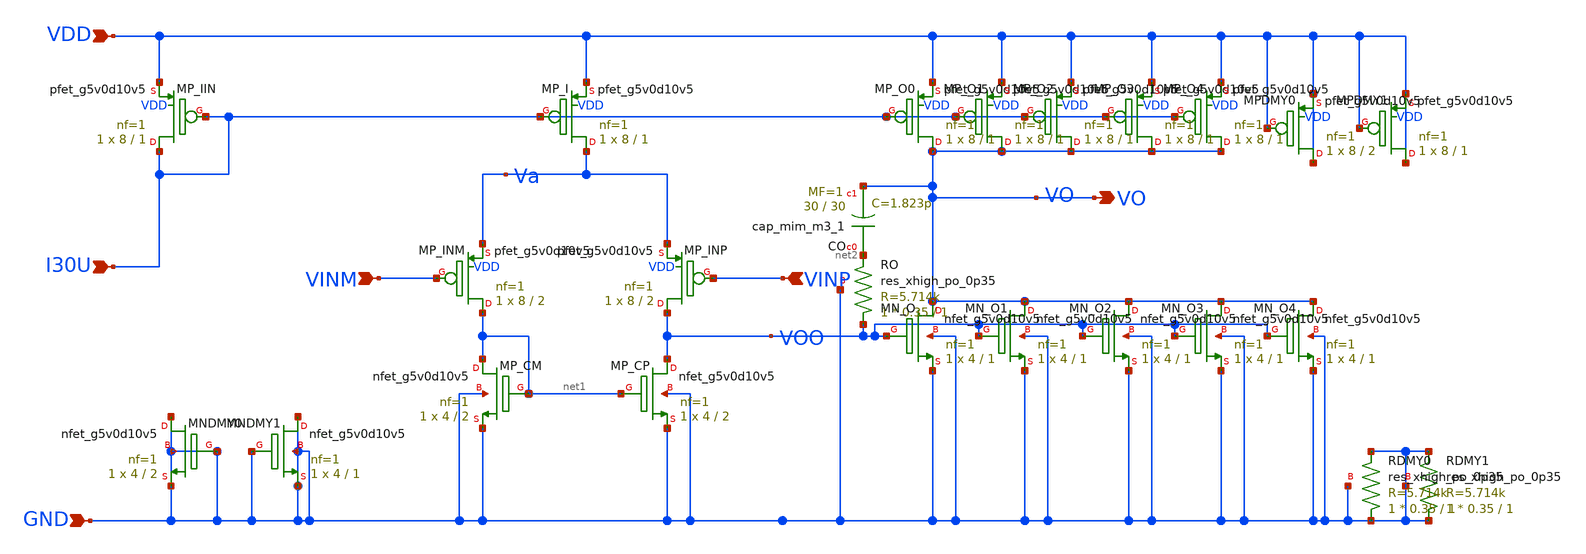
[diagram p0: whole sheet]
** sch_path: design/schematic/opamp3V3_v2.sch
**.subckt opamp3V3_v2 VDD GND VINM VINP VO I30U
*.ipin VDD
*.ipin GND
*.ipin VINM
*.ipin VINP
*.opin VO
*.ipin I30U
XCO net2 VO sky130_fd_pr__cap_mim_m3_1 W=30 L=30 MF=1 m=1
XRO VOO net2 GND sky130_fd_pr__res_xhigh_po_0p35 L=1 mult=1 m=1
XMP_I Va I30U VDD VDD sky130_fd_pr__pfet_g5v0d10v5 L=1 W=8 nf=1 ad='int((nf+1)/2) * W/nf * 0.29' as='int((nf+2)/2) * W/nf * 0.29'
+ pd='2*int((nf+1)/2) * (W/nf + 0.29)' ps='2*int((nf+2)/2) * (W/nf + 0.29)' nrd='0.29 / W' nrs='0.29 / W'
+ sa=0 sb=0 sd=0 mult=1 m=1
XMP_INM net1 VINM Va VDD sky130_fd_pr__pfet_g5v0d10v5 L=2 W=8 nf=1 ad='int((nf+1)/2) * W/nf * 0.29' as='int((nf+2)/2) * W/nf * 0.29'
+ pd='2*int((nf+1)/2) * (W/nf + 0.29)' ps='2*int((nf+2)/2) * (W/nf + 0.29)' nrd='0.29 / W' nrs='0.29 / W'
+ sa=0 sb=0 sd=0 mult=1 m=1
XMP_INP VOO VINP Va VDD sky130_fd_pr__pfet_g5v0d10v5 L=2 W=8 nf=1 ad='int((nf+1)/2) * W/nf * 0.29' as='int((nf+2)/2) * W/nf * 0.29'
+ pd='2*int((nf+1)/2) * (W/nf + 0.29)' ps='2*int((nf+2)/2) * (W/nf + 0.29)' nrd='0.29 / W' nrs='0.29 / W'
+ sa=0 sb=0 sd=0 mult=1 m=1
XMP_CM net1 net1 GND GND sky130_fd_pr__nfet_g5v0d10v5 L=2 W=4 nf=1 ad='int((nf+1)/2) * W/nf * 0.29' as='int((nf+2)/2) * W/nf * 0.29'
+ pd='2*int((nf+1)/2) * (W/nf + 0.29)' ps='2*int((nf+2)/2) * (W/nf + 0.29)' nrd='0.29 / W' nrs='0.29 / W'
+ sa=0 sb=0 sd=0 mult=1 m=1
XMP_CP VOO net1 GND GND sky130_fd_pr__nfet_g5v0d10v5 L=2 W=4 nf=1 ad='int((nf+1)/2) * W/nf * 0.29' as='int((nf+2)/2) * W/nf * 0.29'
+ pd='2*int((nf+1)/2) * (W/nf + 0.29)' ps='2*int((nf+2)/2) * (W/nf + 0.29)' nrd='0.29 / W' nrs='0.29 / W'
+ sa=0 sb=0 sd=0 mult=1 m=1
XMN_O VO VOO GND GND sky130_fd_pr__nfet_g5v0d10v5 L=1 W=4 nf=1 ad='int((nf+1)/2) * W/nf * 0.29' as='int((nf+2)/2) * W/nf * 0.29'
+ pd='2*int((nf+1)/2) * (W/nf + 0.29)' ps='2*int((nf+2)/2) * (W/nf + 0.29)' nrd='0.29 / W' nrs='0.29 / W'
+ sa=0 sb=0 sd=0 mult=1 m=1
XMP_O0 VO I30U VDD VDD sky130_fd_pr__pfet_g5v0d10v5 L=1 W=8 nf=1 ad='int((nf+1)/2) * W/nf * 0.29' as='int((nf+2)/2) * W/nf * 0.29'
+ pd='2*int((nf+1)/2) * (W/nf + 0.29)' ps='2*int((nf+2)/2) * (W/nf + 0.29)' nrd='0.29 / W' nrs='0.29 / W'
+ sa=0 sb=0 sd=0 mult=1 m=1
XMP_O1 VO I30U VDD VDD sky130_fd_pr__pfet_g5v0d10v5 L=1 W=8 nf=1 ad='int((nf+1)/2) * W/nf * 0.29' as='int((nf+2)/2) * W/nf * 0.29'
+ pd='2*int((nf+1)/2) * (W/nf + 0.29)' ps='2*int((nf+2)/2) * (W/nf + 0.29)' nrd='0.29 / W' nrs='0.29 / W'
+ sa=0 sb=0 sd=0 mult=1 m=1
XMP_IIN I30U I30U VDD VDD sky130_fd_pr__pfet_g5v0d10v5 L=1 W=8 nf=1 ad='int((nf+1)/2) * W/nf * 0.29'
+ as='int((nf+2)/2) * W/nf * 0.29' pd='2*int((nf+1)/2) * (W/nf + 0.29)' ps='2*int((nf+2)/2) * (W/nf + 0.29)'
+ nrd='0.29 / W' nrs='0.29 / W' sa=0 sb=0 sd=0 mult=1 m=1
XMN_O1 VO VOO GND GND sky130_fd_pr__nfet_g5v0d10v5 L=1 W=4 nf=1 ad='int((nf+1)/2) * W/nf * 0.29' as='int((nf+2)/2) * W/nf * 0.29'
+ pd='2*int((nf+1)/2) * (W/nf + 0.29)' ps='2*int((nf+2)/2) * (W/nf + 0.29)' nrd='0.29 / W' nrs='0.29 / W'
+ sa=0 sb=0 sd=0 mult=1 m=1
XMPDMY1 VDD VDD VDD VDD sky130_fd_pr__pfet_g5v0d10v5 L=1 W=8 nf=1 ad='int((nf+1)/2) * W/nf * 0.29' as='int((nf+2)/2) * W/nf * 0.29'
+ pd='2*int((nf+1)/2) * (W/nf + 0.29)' ps='2*int((nf+2)/2) * (W/nf + 0.29)' nrd='0.29 / W' nrs='0.29 / W'
+ sa=0 sb=0 sd=0 mult=1 m=1
XMNDMY0 GND GND GND GND sky130_fd_pr__nfet_g5v0d10v5 L=2 W=4 nf=1 ad='int((nf+1)/2) * W/nf * 0.29' as='int((nf+2)/2) * W/nf * 0.29'
+ pd='2*int((nf+1)/2) * (W/nf + 0.29)' ps='2*int((nf+2)/2) * (W/nf + 0.29)' nrd='0.29 / W' nrs='0.29 / W'
+ sa=0 sb=0 sd=0 mult=1 m=1
XMNDMY1 GND GND GND GND sky130_fd_pr__nfet_g5v0d10v5 L=1 W=4 nf=1 ad='int((nf+1)/2) * W/nf * 0.29' as='int((nf+2)/2) * W/nf * 0.29'
+ pd='2*int((nf+1)/2) * (W/nf + 0.29)' ps='2*int((nf+2)/2) * (W/nf + 0.29)' nrd='0.29 / W' nrs='0.29 / W'
+ sa=0 sb=0 sd=0 mult=1 m=1
XRDMY0 GND GND GND sky130_fd_pr__res_xhigh_po_0p35 L=1 mult=1 m=1
XRDMY1 GND GND GND sky130_fd_pr__res_xhigh_po_0p35 L=1 mult=1 m=1
XMPDMY0 VDD VDD VDD VDD sky130_fd_pr__pfet_g5v0d10v5 L=2 W=8 nf=1 ad='int((nf+1)/2) * W/nf * 0.29' as='int((nf+2)/2) * W/nf * 0.29'
+ pd='2*int((nf+1)/2) * (W/nf + 0.29)' ps='2*int((nf+2)/2) * (W/nf + 0.29)' nrd='0.29 / W' nrs='0.29 / W'
+ sa=0 sb=0 sd=0 mult=1 m=1
XMP_O2 VO I30U VDD VDD sky130_fd_pr__pfet_g5v0d10v5 L=1 W=8 nf=1 ad='int((nf+1)/2) * W/nf * 0.29' as='int((nf+2)/2) * W/nf * 0.29'
+ pd='2*int((nf+1)/2) * (W/nf + 0.29)' ps='2*int((nf+2)/2) * (W/nf + 0.29)' nrd='0.29 / W' nrs='0.29 / W'
+ sa=0 sb=0 sd=0 mult=1 m=1
XMP_O3 VO I30U VDD VDD sky130_fd_pr__pfet_g5v0d10v5 L=1 W=8 nf=1 ad='int((nf+1)/2) * W/nf * 0.29' as='int((nf+2)/2) * W/nf * 0.29'
+ pd='2*int((nf+1)/2) * (W/nf + 0.29)' ps='2*int((nf+2)/2) * (W/nf + 0.29)' nrd='0.29 / W' nrs='0.29 / W'
+ sa=0 sb=0 sd=0 mult=1 m=1
XMP_O4 VO I30U VDD VDD sky130_fd_pr__pfet_g5v0d10v5 L=1 W=8 nf=1 ad='int((nf+1)/2) * W/nf * 0.29' as='int((nf+2)/2) * W/nf * 0.29'
+ pd='2*int((nf+1)/2) * (W/nf + 0.29)' ps='2*int((nf+2)/2) * (W/nf + 0.29)' nrd='0.29 / W' nrs='0.29 / W'
+ sa=0 sb=0 sd=0 mult=1 m=1
XMN_O2 VO VOO GND GND sky130_fd_pr__nfet_g5v0d10v5 L=1 W=4 nf=1 ad='int((nf+1)/2) * W/nf * 0.29' as='int((nf+2)/2) * W/nf * 0.29'
+ pd='2*int((nf+1)/2) * (W/nf + 0.29)' ps='2*int((nf+2)/2) * (W/nf + 0.29)' nrd='0.29 / W' nrs='0.29 / W'
+ sa=0 sb=0 sd=0 mult=1 m=1
XMN_O3 VO VOO GND GND sky130_fd_pr__nfet_g5v0d10v5 L=1 W=4 nf=1 ad='int((nf+1)/2) * W/nf * 0.29' as='int((nf+2)/2) * W/nf * 0.29'
+ pd='2*int((nf+1)/2) * (W/nf + 0.29)' ps='2*int((nf+2)/2) * (W/nf + 0.29)' nrd='0.29 / W' nrs='0.29 / W'
+ sa=0 sb=0 sd=0 mult=1 m=1
XMN_O4 VO VOO GND GND sky130_fd_pr__nfet_g5v0d10v5 L=1 W=4 nf=1 ad='int((nf+1)/2) * W/nf * 0.29' as='int((nf+2)/2) * W/nf * 0.29'
+ pd='2*int((nf+1)/2) * (W/nf + 0.29)' ps='2*int((nf+2)/2) * (W/nf + 0.29)' nrd='0.29 / W' nrs='0.29 / W'
+ sa=0 sb=0 sd=0 mult=1 m=1
**.ends
.end
